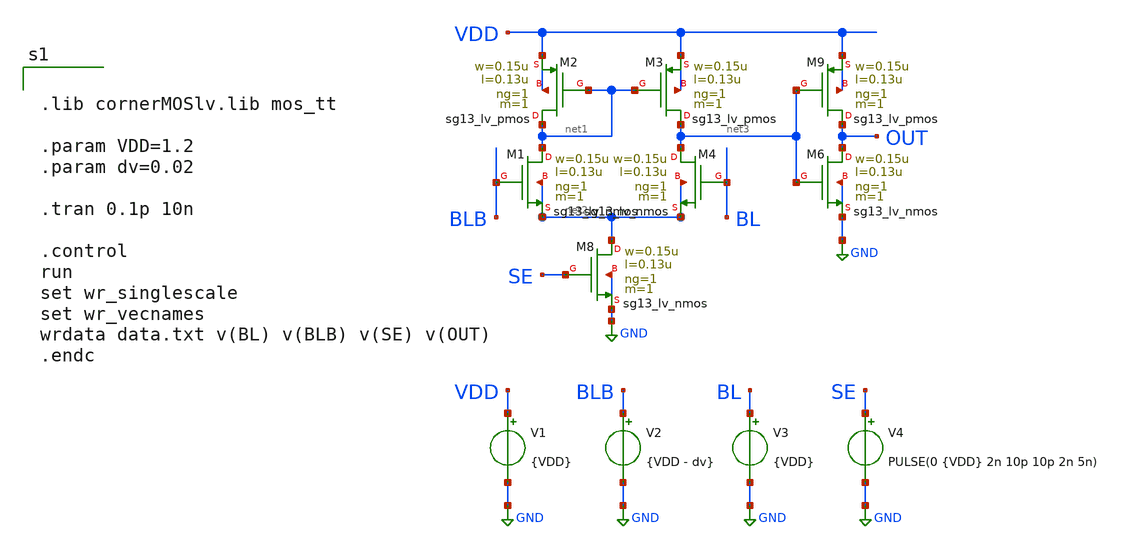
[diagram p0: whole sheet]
** sch_path: xschem/sram-sense-amp.sch
**.subckt sram-sense-amp
V1 VDD GND {VDD}
V2 BLB GND {VDD - dv}
V3 BL GND {VDD}
V4 SE GND PULSE(0 {VDD} 2n 10p 10p 2n 5n)
XM8 net2 SE GND GND sg13_lv_nmos w=0.15u l=0.13u ng=1 m=1 mm_ok=1
XM9 OUT net3 VDD VDD sg13_lv_pmos w=0.15u l=0.13u ng=1 m=1 mm_ok=1
XM1 net1 BLB net2 net2 sg13_lv_nmos w=0.15u l=0.13u ng=1 m=1 mm_ok=1
XM3 net3 net1 VDD VDD sg13_lv_pmos w=0.15u l=0.13u ng=1 m=1 mm_ok=1
XM2 net1 net1 VDD VDD sg13_lv_pmos w=0.15u l=0.13u ng=1 m=1 mm_ok=1
XM6 OUT net3 GND GND sg13_lv_nmos w=0.15u l=0.13u ng=1 m=1 mm_ok=1
XM4 net3 BL net2 net2 sg13_lv_nmos w=0.15u l=0.13u ng=1 m=1 mm_ok=1
**** begin user architecture code


.lib cornerMOSlv.lib mos_tt

.param VDD=1.2
.param dv=0.02

.tran 0.1p 10n

.control
run
set wr_singlescale
set wr_vecnames
wrdata data.txt v(BL) v(BLB) v(SE) v(OUT)
.endc


**** end user architecture code
**.ends
.GLOBAL GND
.end
